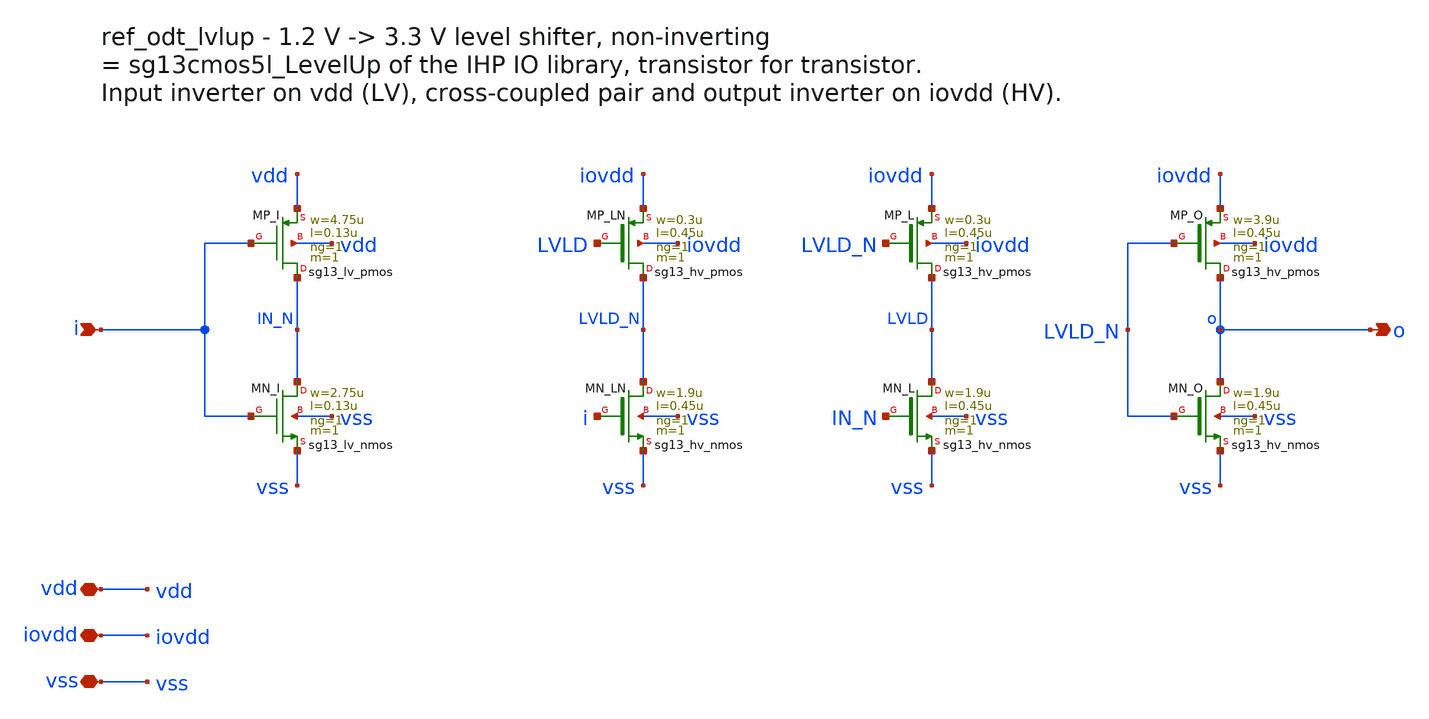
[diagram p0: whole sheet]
** sch_path: macros/ref_odt/schematic/xschem/ref_odt_lvlup.sch
**.subckt ref_odt_lvlup i o vdd iovdd vss
*.ipin i
*.opin o
*.iopin vdd
*.iopin iovdd
*.iopin vss
XMP_I IN_N i vdd vdd sg13_lv_pmos w=4.75u l=0.13u ng=1 m=1 mm_ok=1
XMN_I IN_N i vss vss sg13_lv_nmos w=2.75u l=0.13u ng=1 m=1 mm_ok=1
XMP_LN LVLD_N LVLD iovdd iovdd sg13_hv_pmos w=0.3u l=0.45u ng=1 m=1 mm_ok=1
XMN_LN LVLD_N i vss vss sg13_hv_nmos w=1.9u l=0.45u ng=1 m=1 mm_ok=1
XMP_L LVLD LVLD_N iovdd iovdd sg13_hv_pmos w=0.3u l=0.45u ng=1 m=1 mm_ok=1
XMN_L LVLD IN_N vss vss sg13_hv_nmos w=1.9u l=0.45u ng=1 m=1 mm_ok=1
XMP_O o LVLD_N iovdd iovdd sg13_hv_pmos w=3.9u l=0.45u ng=1 m=1 mm_ok=1
XMN_O o LVLD_N vss vss sg13_hv_nmos w=1.9u l=0.45u ng=1 m=1 mm_ok=1
**.ends
.end
